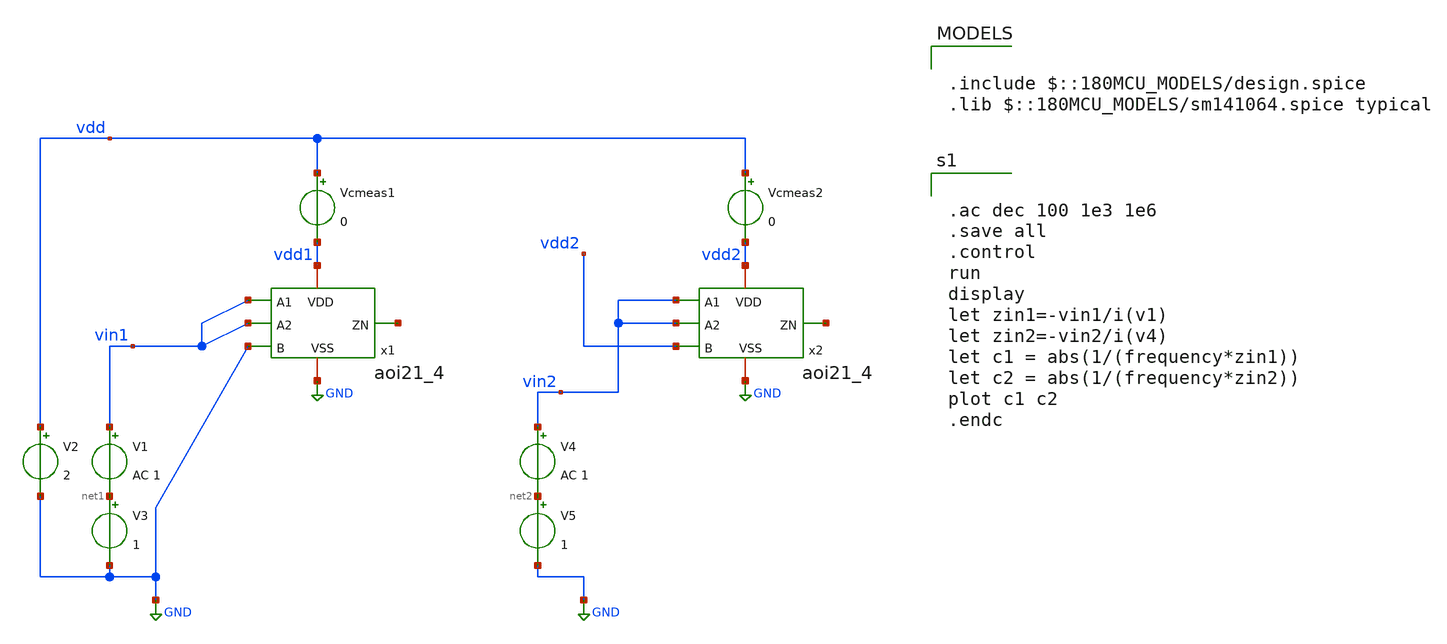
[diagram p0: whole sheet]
** sch_path: xschem/aoi_cap_test.sch
**.subckt aoi_cap_test
V1 vin1 net1 AC 1
V2 vdd GND 2
V3 net1 GND 1
V4 vin2 net2 AC 1
V5 net2 GND 1
Vcmeas1 vdd vdd1 0
Vcmeas2 vdd vdd2 0
x1 vdd1 vin1 net3 vin1 GND GND aoi21_4
x2 vdd2 vin2 net4 vin2 vdd2 GND aoi21_4
**** begin user architecture code


.ac dec 100 1e3 1e6
.save all
.control
run
display
let zin1=-vin1/i(v1)
let zin2=-vin2/i(v4)
let c1 = abs(1/(frequency*zin1))
let c2 = abs(1/(frequency*zin2))
plot c1 c2
.endc



.include $::180MCU_MODELS/design.spice
.lib $::180MCU_MODELS/sm141064.spice typical

**** end user architecture code
**.ends

* expanding   symbol:  aoi21_4.sym # of pins=6
** sym_path: xschem/aoi21_4.sym
** sch_path: xschem/aoi21_4.sch
.subckt aoi21_4 VDD A1 ZN A2 B VSS
*.ipin A1
*.ipin A2
*.ipin B
*.opin ZN
*.iopin VDD
*.iopin VSS
**** begin user architecture code

.subckt aoi21_4_flat A1 A2 B ZN VDD VSS
X0 a_288_68# A2 VSS VSUBS nmos_6p0 w=0.82u l=0.6u
X1 a_1072_68# A2 VSS VSUBS nmos_6p0 w=0.82u l=0.6u
X2 VSS B ZN VSUBS nmos_6p0 w=0.51u l=0.6u
X3 a_76_476# A1 ZN w_n86_352# pmos_6p0 w=1.2u l=0.5u
X4 ZN A1 a_288_68# VSUBS nmos_6p0 w=0.82u l=0.6u
X5 ZN A1 a_76_476# w_n86_352# pmos_6p0 w=1.2u l=0.5u
X6 a_76_476# A2 ZN w_n86_352# pmos_6p0 w=1.2u l=0.5u
X7 a_76_476# B VDD w_n86_352# pmos_6p0 w=1.2u l=0.5u
X8 ZN B VSS VSUBS nmos_6p0 w=0.51u l=0.6u
X9 a_680_68# A1 ZN VSUBS nmos_6p0 w=0.82u l=0.6u
X10 VDD B a_76_476# w_n86_352# pmos_6p0 w=1.2u l=0.5u
X11 VDD B a_76_476# w_n86_352# pmos_6p0 w=1.2u l=0.5u
X12 a_76_476# B VDD w_n86_352# pmos_6p0 w=1.2u l=0.5u
X13 ZN B VSS VSUBS nmos_6p0 w=0.51u l=0.6u
X14 ZN A2 a_76_476# w_n86_352# pmos_6p0 w=1.2u l=0.5u
X15 a_76_476# A1 ZN w_n86_352# pmos_6p0 w=1.2u l=0.5u
X16 a_1464_68# A1 ZN VSUBS nmos_6p0 w=0.82u l=0.6u
X17 ZN A1 a_76_476# w_n86_352# pmos_6p0 w=1.2u l=0.5u
X18 VSS A2 a_1464_68# VSUBS nmos_6p0 w=0.82u l=0.6u
X19 a_76_476# A2 ZN w_n86_352# pmos_6p0 w=1.2u l=0.5u
X20 VSS A2 a_680_68# VSUBS nmos_6p0 w=0.82u l=0.6u
X21 ZN A2 a_76_476# w_n86_352# pmos_6p0 w=1.2u l=0.5u
X22 VSS B ZN VSUBS nmos_6p0 w=0.51u l=0.6u
X23 ZN A1 a_1072_68# VSUBS nmos_6p0 w=0.82u l=0.6u
C0 w_n86_352# VSUBS 4.44fF $ **FLOATING
.ends

XDUT A1 A2 B ZN VDD VSS aoi21_4_flat


**** end user architecture code
.ends

.GLOBAL GND
.end
